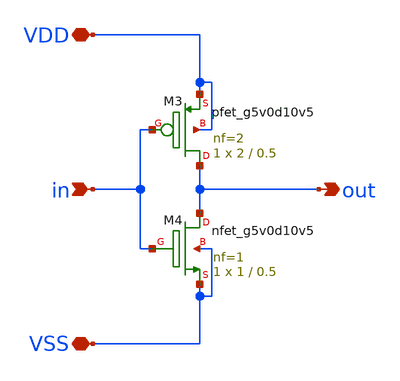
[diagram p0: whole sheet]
** sch_path: Sample&Hold/schematic/inverter_monte_carlo_mismatch/inverter.sch
**.subckt inverter VDD VSS in out
*.iopin VDD
*.iopin VSS
*.ipin in
*.opin out
XM3 out in VDD VDD sky130_fd_pr__pfet_g5v0d10v5 L=0.5 W=2 nf=2 ad='int((nf+1)/2) * W/nf * 0.29' as='int((nf+2)/2) * W/nf * 0.29'
+ pd='2*int((nf+1)/2) * (W/nf + 0.29)' ps='2*int((nf+2)/2) * (W/nf + 0.29)' nrd='0.29 / W' nrs='0.29 / W'
+ sa=0 sb=0 sd=0 mult=1 m=1
XM4 out in VSS VSS sky130_fd_pr__nfet_g5v0d10v5 L=0.5 W=1 nf=1 ad='int((nf+1)/2) * W/nf * 0.29' as='int((nf+2)/2) * W/nf * 0.29'
+ pd='2*int((nf+1)/2) * (W/nf + 0.29)' ps='2*int((nf+2)/2) * (W/nf + 0.29)' nrd='0.29 / W' nrs='0.29 / W'
+ sa=0 sb=0 sd=0 mult=1 m=1
**.ends
.end
